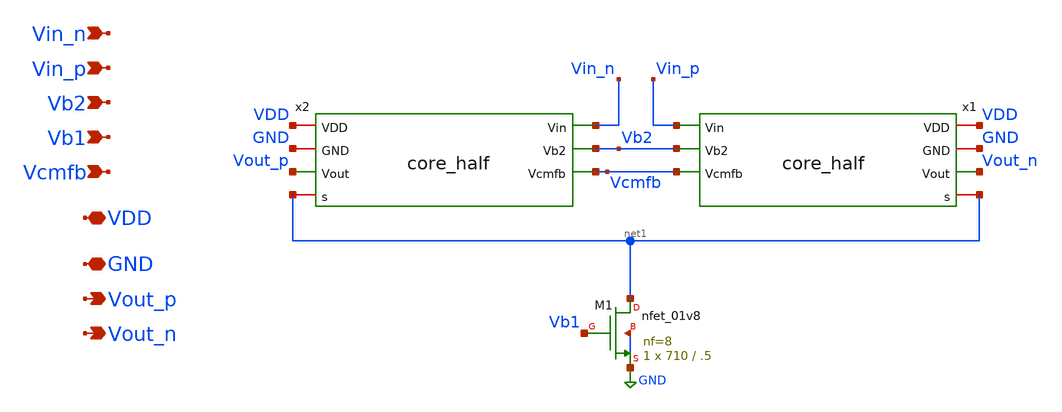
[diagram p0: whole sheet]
** sch_path: xschem/core.sch
**.subckt core Vb2 Vcmfb VDD GND Vout_p Vin_p Vin_n Vout_n Vb1
*.ipin Vb2
*.ipin Vcmfb
*.iopin VDD
*.iopin GND
*.opin Vout_p
*.ipin Vin_p
*.ipin Vin_n
*.opin Vout_n
*.ipin Vb1
XM1 net1 Vb1 GND GND sky130_fd_pr__nfet_01v8 L=.5 W=710 nf=8 ad='int((nf+1)/2) * W/nf * 0.29' as='int((nf+2)/2) * W/nf * 0.29'
+ pd='2*int((nf+1)/2) * (W/nf + 0.29)' ps='2*int((nf+2)/2) * (W/nf + 0.29)' nrd='0.29 / W' nrs='0.29 / W'
+ sa=0 sb=0 sd=0 mult=1 m=1
x1 Vin_p Vb2 Vcmfb VDD GND Vout_n net1 core_half
x2 Vin_n Vb2 Vcmfb VDD GND Vout_p net1 core_half
**.ends

* expanding   symbol:  tia_post_approval/schem/core_half.sym # of pins=7
** sym_path: tia_post_approval/schem/core_half.sym
** sch_path: tia_post_approval/schem/core_half.sch
.subckt core_half Vin Vb2 Vcmfb VDD GND Vout s
*.ipin Vb2
*.ipin Vcmfb
*.iopin VDD
*.iopin GND
*.opin Vout
*.iopin s
*.ipin Vin
XM3 Vout Vin s GND sky130_fd_pr__nfet_01v8 L=0.15 W=150 nf=4 ad='int((nf+1)/2) * W/nf * 0.29' as='int((nf+2)/2) * W/nf * 0.29'
+ pd='2*int((nf+1)/2) * (W/nf + 0.29)' ps='2*int((nf+2)/2) * (W/nf + 0.29)' nrd='0.29 / W' nrs='0.29 / W'
+ sa=0 sb=0 sd=0 mult=1 m=1
XM5 Vout Vcmfb VDD VDD sky130_fd_pr__pfet_01v8 L=0.18 W=112 nf=5 ad='int((nf+1)/2) * W/nf * 0.29' as='int((nf+2)/2) * W/nf * 0.29'
+ pd='2*int((nf+1)/2) * (W/nf + 0.29)' ps='2*int((nf+2)/2) * (W/nf + 0.29)' nrd='0.29 / W' nrs='0.29 / W'
+ sa=0 sb=0 sd=0 mult=1 m=1
XM25 Vout Vb2 VDD VDD sky130_fd_pr__pfet_01v8 L=0.18 W=448 nf=15 ad='int((nf+1)/2) * W/nf * 0.29' as='int((nf+2)/2) * W/nf * 0.29'
+ pd='2*int((nf+1)/2) * (W/nf + 0.29)' ps='2*int((nf+2)/2) * (W/nf + 0.29)' nrd='0.29 / W' nrs='0.29 / W'
+ sa=0 sb=0 sd=0 mult=1 m=1
.ends

.GLOBAL GND
.end
